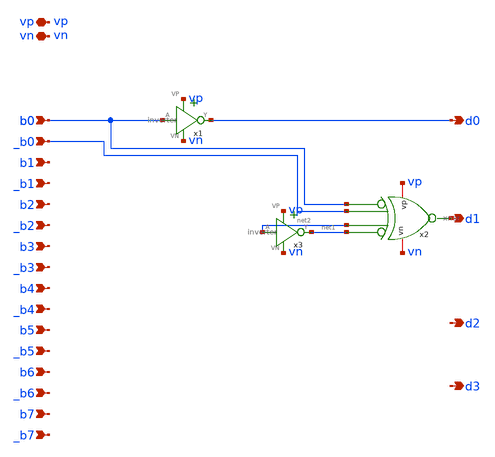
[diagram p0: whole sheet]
** sch_path: xschem/sin_cl.sch
**.subckt sin_cl b0 _b0 b1 _b1 b2 _b2 b3 _b3 b4 _b4 b5 _b5 b6 _b6 b7 _b7 b0 d0 d1 d2 d3 vp vn
*.ipin b0
*.ipin _b0
*.ipin b1
*.ipin _b1
*.ipin b2
*.ipin _b2
*.ipin b3
*.ipin _b3
*.ipin b4
*.ipin _b4
*.ipin b5
*.ipin _b5
*.ipin b6
*.ipin _b6
*.ipin b7
*.ipin _b7
*.ipin b0
*.opin d0
*.opin d1
*.opin d2
*.opin d3
*.iopin vp
*.iopin vn
x1 vp b0 d0 vn inverter
x2 vp _b0 net2 d1 b0 net1 vn xnor
x3 vp net2 net1 vn inverter
**.ends

* expanding   symbol:  /home/madvlsi/dev/git/magic-dds/xschem/other_project_files/inverter.sym # of
*+ pins=4
** sym_path: xschem/other_project_files/inverter.sym
** sch_path: xschem/other_project_files/inverter.sch
.subckt inverter VP A Y VN
*.iopin VP
*.iopin VN
*.ipin A
*.opin Y
XM1 Y A VN VN sky130_fd_pr__nfet_01v8 L=0.15 W=1 nf=1 ad='int((nf+1)/2) * W/nf * 0.29' as='int((nf+2)/2) * W/nf * 0.29'
+ pd='2*int((nf+1)/2) * (W/nf + 0.29)' ps='2*int((nf+2)/2) * (W/nf + 0.29)' nrd='0.29 / W' nrs='0.29 / W'
+ sa=0 sb=0 sd=0 mult=1 m=1
XM2 Y A VP VP sky130_fd_pr__pfet_01v8 L=0.15 W=4 nf=1 ad='int((nf+1)/2) * W/nf * 0.29' as='int((nf+2)/2) * W/nf * 0.29'
+ pd='2*int((nf+1)/2) * (W/nf + 0.29)' ps='2*int((nf+2)/2) * (W/nf + 0.29)' nrd='0.29 / W' nrs='0.29 / W'
+ sa=0 sb=0 sd=0 mult=1 m=1
.ends


* expanding   symbol:  /home/madvlsi/dev/git/magic-dds/xschem/logic_gates/xnor.sym # of pins=7
** sym_path: xschem/logic_gates/xnor.sym
** sch_path: xschem/logic_gates/xnor.sch
.subckt xnor vp A B Y _A _B vn
*.iopin vp
*.iopin vn
*.ipin A
*.ipin B
*.ipin _A
*.ipin _B
*.opin Y
x1 vn A B net1 vp nand
x2 vn _A _B net2 vp nand
x3 vn net1 net2 Y vp nand
.ends


* expanding   symbol:  /home/madvlsi/dev/git/magic-dds/xschem/logic_gates/nand.sym # of pins=5
** sym_path: xschem/logic_gates/nand.sym
** sch_path: xschem/logic_gates/nand.sch
.subckt nand VN A B Y VP
*.iopin VP
*.iopin VN
*.ipin A
*.ipin B
*.opin Y
XM1 Y A net1 GND sky130_fd_pr__nfet_01v8 L=0.15 W=1 nf=1 ad='int((nf+1)/2) * W/nf * 0.29' as='int((nf+2)/2) * W/nf * 0.29'
+ pd='2*int((nf+1)/2) * (W/nf + 0.29)' ps='2*int((nf+2)/2) * (W/nf + 0.29)' nrd='0.29 / W' nrs='0.29 / W'
+ sa=0 sb=0 sd=0 mult=1 m=1
XM2 net1 B VN GND sky130_fd_pr__nfet_01v8 L=0.15 W=1 nf=1 ad='int((nf+1)/2) * W/nf * 0.29' as='int((nf+2)/2) * W/nf * 0.29'
+ pd='2*int((nf+1)/2) * (W/nf + 0.29)' ps='2*int((nf+2)/2) * (W/nf + 0.29)' nrd='0.29 / W' nrs='0.29 / W'
+ sa=0 sb=0 sd=0 mult=1 m=1
XM3 Y A VP VDD sky130_fd_pr__pfet_01v8 L=0.15 W=1 nf=1 ad='int((nf+1)/2) * W/nf * 0.29' as='int((nf+2)/2) * W/nf * 0.29'
+ pd='2*int((nf+1)/2) * (W/nf + 0.29)' ps='2*int((nf+2)/2) * (W/nf + 0.29)' nrd='0.29 / W' nrs='0.29 / W'
+ sa=0 sb=0 sd=0 mult=1 m=1
XM4 Y B VP VDD sky130_fd_pr__pfet_01v8 L=0.15 W=1 nf=1 ad='int((nf+1)/2) * W/nf * 0.29' as='int((nf+2)/2) * W/nf * 0.29'
+ pd='2*int((nf+1)/2) * (W/nf + 0.29)' ps='2*int((nf+2)/2) * (W/nf + 0.29)' nrd='0.29 / W' nrs='0.29 / W'
+ sa=0 sb=0 sd=0 mult=1 m=1
.ends

.end
